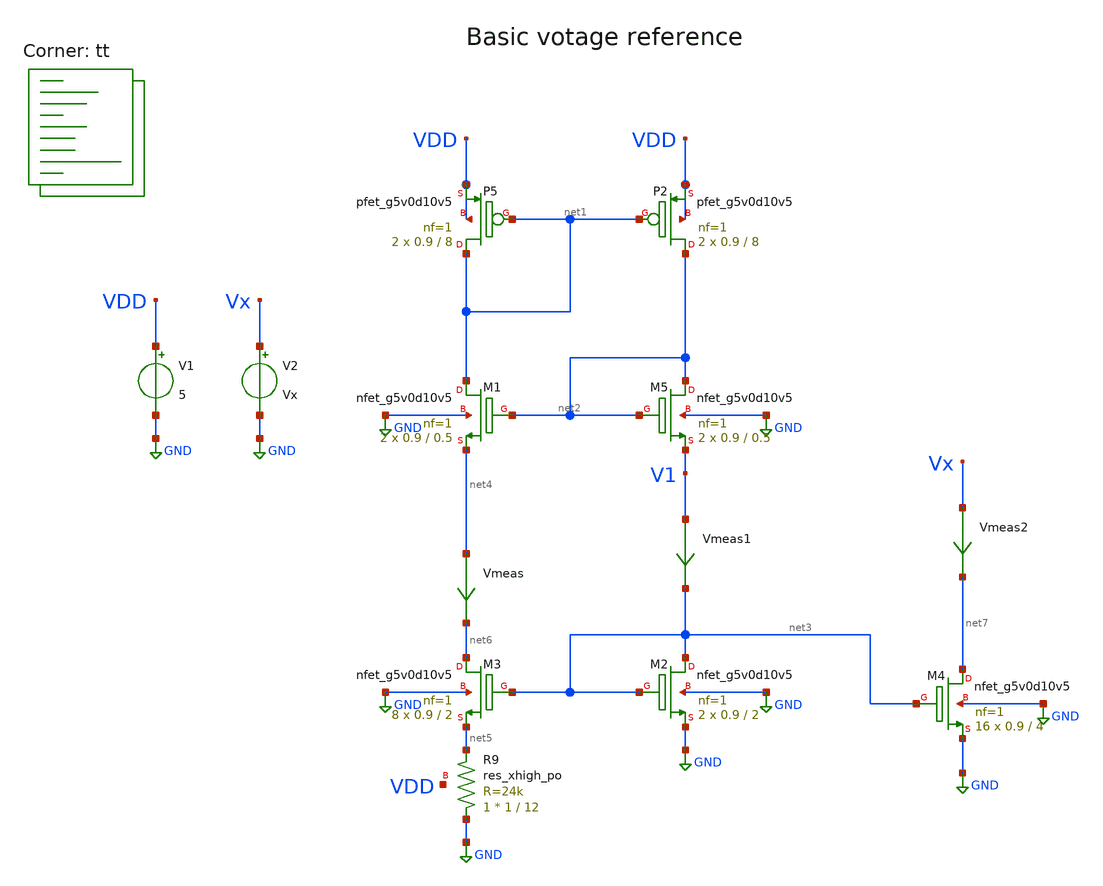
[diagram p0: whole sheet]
** sch_path: my_projects/V_REF/basic_bandgap/basic_PTAT.sch
**.subckt basic_PTAT
V1 VDD GND 5
XP5 net1 net1 VDD VDD sky130_fd_pr__pfet_g5v0d10v5 L=8 W=0.9 nf=1 ad='int((1 + 1)/2) * 0.9 / 1 * 0.29'
+ as='int((1 + 2)/2) * 0.9 / 1 * 0.29' pd='2*int((1 + 1)/2) * (0.9 / 1 + 0.29)' ps='2*int((1 + 2)/2) * (0.9 / 1 + 0.29)'
+ nrd='0.29 / 0.9 ' nrs='0.29 / 0.9 ' sa=0 sb=0 sd=0 mult=2 m=2
XP2 net2 net1 VDD VDD sky130_fd_pr__pfet_g5v0d10v5 L=8 W=0.9 nf=1 ad='int((1 + 1)/2) * 0.9 / 1 * 0.29'
+ as='int((1 + 2)/2) * 0.9 / 1 * 0.29' pd='2*int((1 + 1)/2) * (0.9 / 1 + 0.29)' ps='2*int((1 + 2)/2) * (0.9 / 1 + 0.29)'
+ nrd='0.29 / 0.9 ' nrs='0.29 / 0.9 ' sa=0 sb=0 sd=0 mult=2 m=2
XM5 net2 net2 V1 GND sky130_fd_pr__nfet_g5v0d10v5 L=0.5 W=0.9 nf=1 ad='int((1 + 1)/2) * 0.9 / 1 * 0.29'
+ as='int((1 + 2)/2) * 0.9 / 1 * 0.29' pd='2*int((1 + 1)/2) * (0.9 / 1 + 0.29)' ps='2*int((1 + 2)/2) * (0.9 / 1 + 0.29)'
+ nrd='0.29 / 0.9 ' nrs='0.29 / 0.9 ' sa=0 sb=0 sd=0 mult=2 m=2
XM1 net1 net2 net4 GND sky130_fd_pr__nfet_g5v0d10v5 L=0.5 W=0.9 nf=1 ad='int((1 + 1)/2) * 0.9 / 1 * 0.29'
+ as='int((1 + 2)/2) * 0.9 / 1 * 0.29' pd='2*int((1 + 1)/2) * (0.9 / 1 + 0.29)' ps='2*int((1 + 2)/2) * (0.9 / 1 + 0.29)'
+ nrd='0.29 / 0.9 ' nrs='0.29 / 0.9 ' sa=0 sb=0 sd=0 mult=2 m=2
XM2 net3 net3 GND GND sky130_fd_pr__nfet_g5v0d10v5 L=2 W=0.9 nf=1 ad='int((1 + 1)/2) * 0.9 / 1 * 0.29'
+ as='int((1 + 2)/2) * 0.9 / 1 * 0.29' pd='2*int((1 + 1)/2) * (0.9 / 1 + 0.29)' ps='2*int((1 + 2)/2) * (0.9 / 1 + 0.29)'
+ nrd='0.29 / 0.9 ' nrs='0.29 / 0.9 ' sa=0 sb=0 sd=0 mult=2 m=2
XM3 net6 net3 net5 GND sky130_fd_pr__nfet_g5v0d10v5 L=2 W=0.9 nf=1 ad='int((1 + 1)/2) * 0.9 / 1 * 0.29'
+ as='int((1 + 2)/2) * 0.9 / 1 * 0.29' pd='2*int((1 + 1)/2) * (0.9 / 1 + 0.29)' ps='2*int((1 + 2)/2) * (0.9 / 1 + 0.29)'
+ nrd='0.29 / 0.9 ' nrs='0.29 / 0.9 ' sa=0 sb=0 sd=0 mult=8 m=8
XR9 GND net5 VDD sky130_fd_pr__res_xhigh_po W=1 L=12 mult=1 m=1
Vmeas net4 net6 0
.save i(vmeas)
Vmeas1 V1 net3 0
.save i(vmeas1)
XM4 net7 net3 GND GND sky130_fd_pr__nfet_g5v0d10v5 L=4 W=0.9 nf=1 ad='int((1 + 1)/2) * 0.9 / 1 * 0.29'
+ as='int((1 + 2)/2) * 0.9 / 1 * 0.29' pd='2*int((1 + 1)/2) * (0.9 / 1 + 0.29)' ps='2*int((1 + 2)/2) * (0.9 / 1 + 0.29)'
+ nrd='0.29 / 0.9 ' nrs='0.29 / 0.9 ' sa=0 sb=0 sd=0 mult=16 m=16
Vmeas2 Vx net7 0
.save i(vmeas2)
V2 Vx GND Vx
**** begin user architecture code
.lib $::SKYWATER_MODELS/sky130.lib.spice tt

**************************************************************
**************************************************************
**************************************************************
**************************************************************
**************************************************************
*LIBs*********************************************************
**************************************************************
**************************************************************
**************************************************************
**************************************************************
**************************************************************
*.lib $::SKYWATER_MODELS/sky130.lib.spice tt
* chose the corners in the corner file
* tt_mm for mismatch
* ss ff sf fs standart corners
* ll hh lh hl capacitor and resistors corners
* mc for total process variation including corners
**************************************************************
**************************************************************
**************************************************************
**************************************************************
**************************************************************
*Corners/montecarlo options***********************************
**************************************************************
**************************************************************
**************************************************************
**************************************************************
**************************************************************
.TEMP 125
**************************************************************
**************************************************************
**************************************************************
**************************************************************
*SIMULATION and Plots*****************************************
**************************************************************
**************************************************************
**************************************************************
**************************************************************
.param Vx = 0
.control
save all
dc TEMP -40 125 1
*dc simulation
plot (V(V1))
plot deriv(V(V1))
plot i(Vmeas) i(Vmeas1)
dc V2 0 5 0.001
plot i(Vmeas2)
.endc

**** end user architecture code
**.ends
.GLOBAL GND
.end
